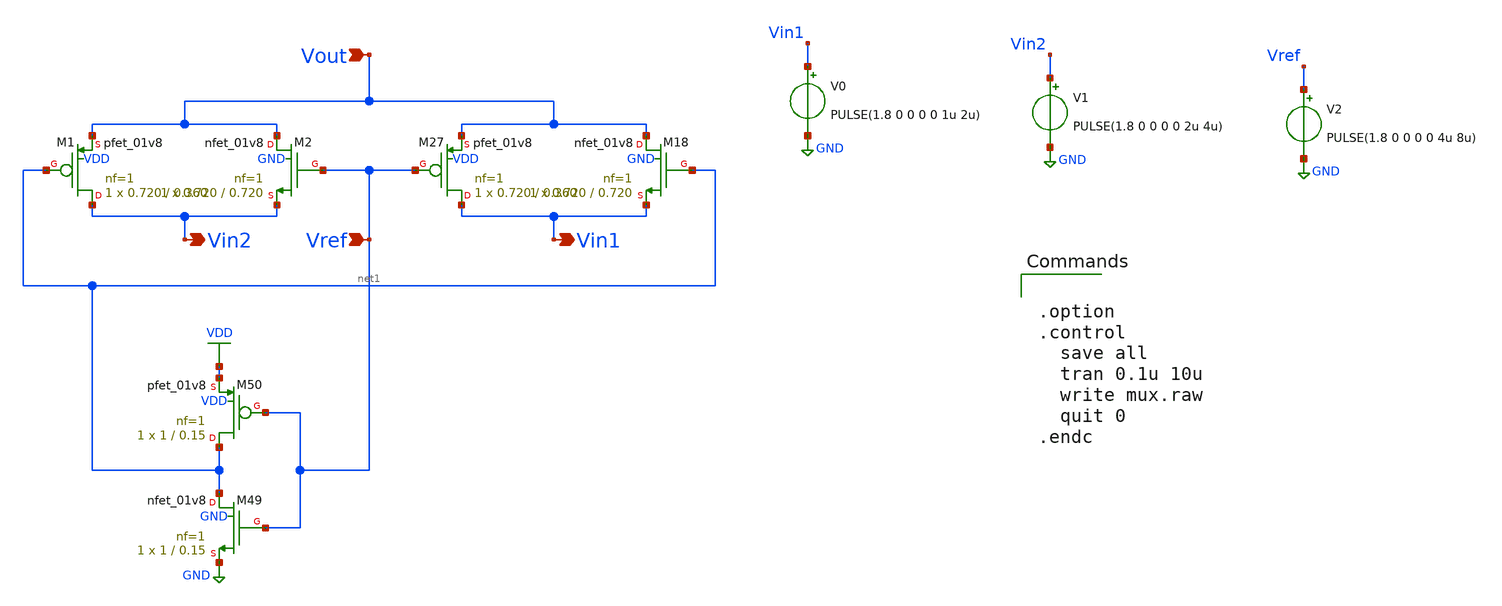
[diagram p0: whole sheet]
** sch_path: xschem/mux.sch
**.subckt mux Vin1 Vref Vout Vin2
*.opin Vin1
*.ipin Vref
*.ipin Vout
*.opin Vin2
XM27 Vin1 Vref Vout VDD sky130_fd_pr__pfet_01v8 L=0.360 W=0.720 nf=1 ad='int((1 + 1)/2) * 0.720 / 1 * 0.29'
+ as='int((1 + 2)/2) * 0.720 / 1 * 0.29' pd='2*int((1 + 1)/2) * (0.720 / 1 + 0.29)' ps='2*int((1 + 2)/2) * (0.720 / 1 + 0.29)'
+ nrd='0.29 / 0.720 ' nrs='0.29 / 0.720 ' sa=0 sb=0 sd=0 mult=1 m=1
XM18 Vout net1 Vin1 GND sky130_fd_pr__nfet_01v8 L=0.720 W=0.720 nf=1 ad='int((nf+1)/2) * W/nf * 0.29'
+ as='int((nf+2)/2) * W/nf * 0.29' pd='2*int((nf+1)/2) * (W/nf + 0.29)' ps='2*int((nf+2)/2) * (W/nf + 0.29)'
+ nrd='0.29 / W' nrs='0.29 / W' sa=0 sb=0 sd=0 mult=1 m=1
XM1 Vin2 net1 Vout VDD sky130_fd_pr__pfet_01v8 L=0.360 W=0.720 nf=1 ad='int((1 + 1)/2) * 0.720 / 1 * 0.29'
+ as='int((1 + 2)/2) * 0.720 / 1 * 0.29' pd='2*int((1 + 1)/2) * (0.720 / 1 + 0.29)' ps='2*int((1 + 2)/2) * (0.720 / 1 + 0.29)'
+ nrd='0.29 / 0.720 ' nrs='0.29 / 0.720 ' sa=0 sb=0 sd=0 mult=1 m=1
XM2 Vout Vref Vin2 GND sky130_fd_pr__nfet_01v8 L=0.720 W=0.720 nf=1 ad='int((nf+1)/2) * W/nf * 0.29'
+ as='int((nf+2)/2) * W/nf * 0.29' pd='2*int((nf+1)/2) * (W/nf + 0.29)' ps='2*int((nf+2)/2) * (W/nf + 0.29)'
+ nrd='0.29 / W' nrs='0.29 / W' sa=0 sb=0 sd=0 mult=1 m=1
XM49 net1 Vref GND GND sky130_fd_pr__nfet_01v8 L=0.15 W=1 nf=1 ad='int((nf+1)/2) * W/nf * 0.29' as='int((nf+2)/2) * W/nf * 0.29'
+ pd='2*int((nf+1)/2) * (W/nf + 0.29)' ps='2*int((nf+2)/2) * (W/nf + 0.29)' nrd='0.29 / W' nrs='0.29 / W'
+ sa=0 sb=0 sd=0 mult=1 m=1
XM50 net1 Vref VDD VDD sky130_fd_pr__pfet_01v8 L=0.15 W=1 nf=1 ad='int((1 + 1)/2) * 1 / 1 * 0.29' as='int((1 + 2)/2) * 1 / 1 * 0.29'
+ pd='2*int((1 + 1)/2) * (1 / 1 + 0.29)' ps='2*int((1 + 2)/2) * (1 / 1 + 0.29)' nrd='0.29 / 1 ' nrs='0.29 / 1 '
+ sa=0 sb=0 sd=0 mult=1 m=1
V0 Vin1 GND PULSE(1.8 0 0 0 0 1u 2u)
V1 Vin2 GND PULSE(1.8 0 0 0 0 2u 4u)
V2 Vref GND PULSE(1.8 0 0 0 0 4u 8u)
**** begin user architecture code

** opencircuitdesign pdks install
.lib $::SKYWATER_MODELS/sky130.lib.spice tt




.option
.control
  save all
  tran 0.1u 10u
  write mux.raw
  quit 0
.endc


**** end user architecture code
**.ends
.GLOBAL GND
.GLOBAL VDD
.end
